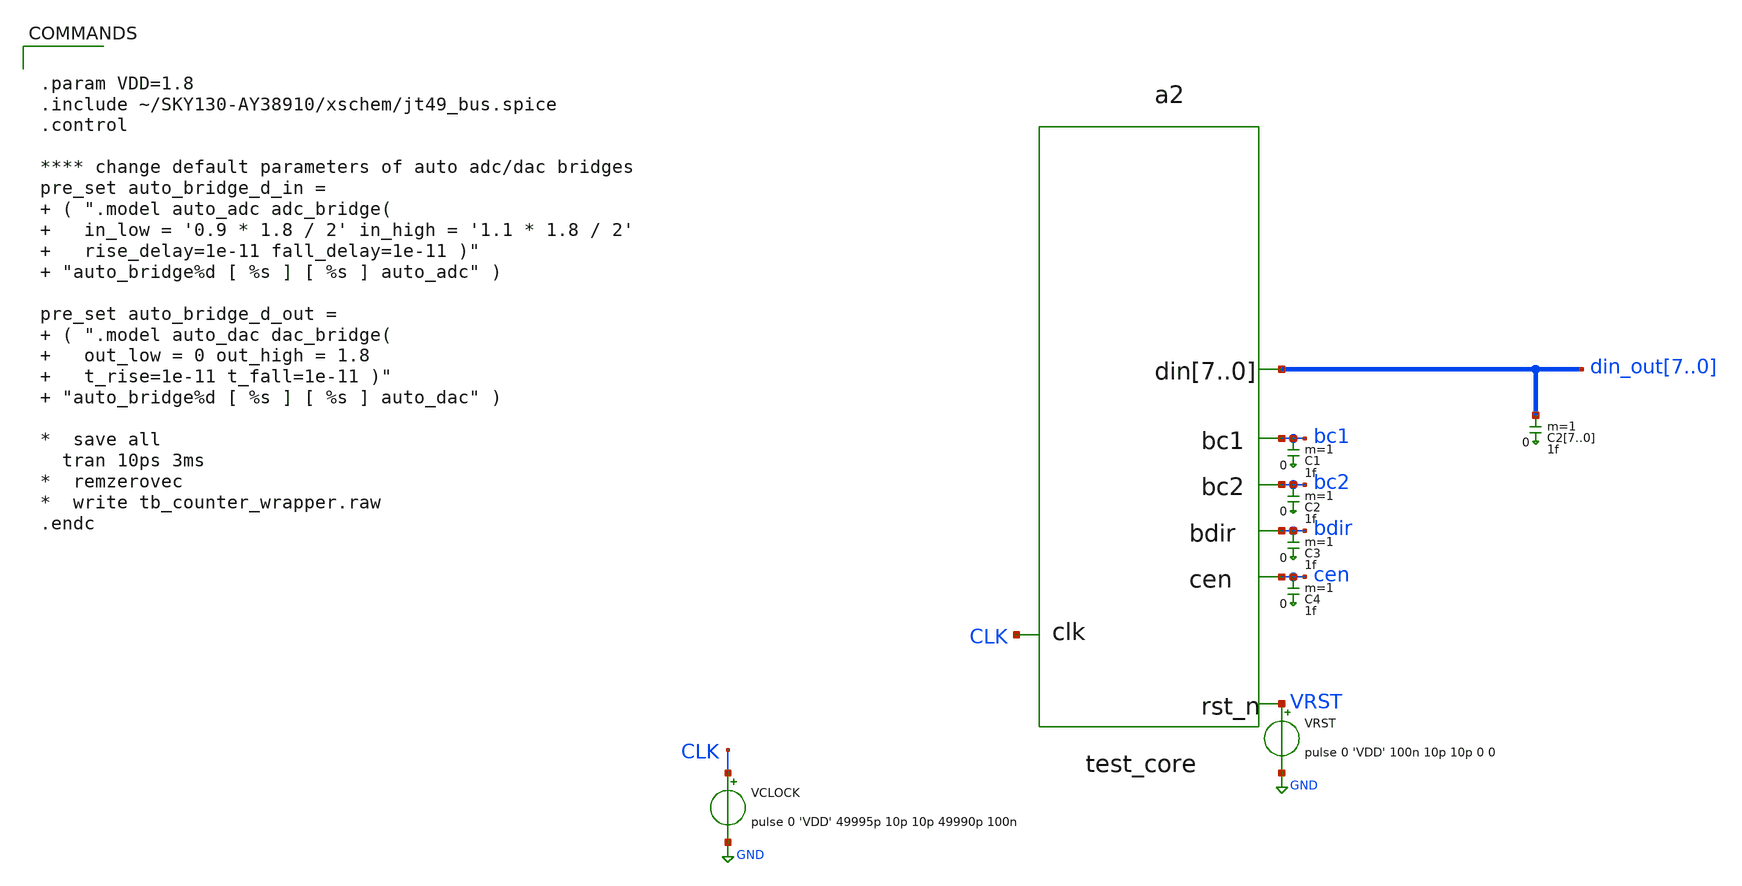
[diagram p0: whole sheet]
** sch_path: xschem/tb_test_core.sch
**.subckt tb_test_core
VRST VRST GND pulse 0 'VDD' 100n 10p 10p 0 0
a2 [ CLK VRST ] [ cen bdir bc1 bc2 din_out7 din_out6 din_out5 din_out4 din_out3 din_out2 din_out1
+ din_out0 ] test_core
VCLOCK CLK GND pulse 0 'VDD' 49995p 10p 10p 49990p 100n
C27 din_out7 0 1f m=1
C26 din_out6 0 1f m=1
C25 din_out5 0 1f m=1
C24 din_out4 0 1f m=1
C23 din_out3 0 1f m=1
C22 din_out2 0 1f m=1
C21 din_out1 0 1f m=1
C20 din_out0 0 1f m=1
C1 bc1 0 1f m=1
C2 bc2 0 1f m=1
C3 bdir 0 1f m=1
C4 cen 0 1f m=1
**** begin user architecture code


.param VDD=1.8
.include ~/SKY130-AY38910/xschem/jt49_bus.spice
.control

**** change default parameters of auto adc/dac bridges
pre_set auto_bridge_d_in =  ( ".model auto_adc adc_bridge(    in_low = '0.9 * 1.8 / 2' in_high = '1.1 * 1.8 / 2'
+    rise_delay=1e-11 fall_delay=1e-11 )"  "auto_bridge%d [ %s ] [ %s ] auto_adc" )

pre_set auto_bridge_d_out =  ( ".model auto_dac dac_bridge(    out_low = 0 out_high = 1.8
+    t_rise=1e-11 t_fall=1e-11 )"  "auto_bridge%d [ %s ] [ %s ] auto_dac" )

*  save all
  tran 10ps 3ms
*  remzerovec
*  write tb_counter_wrapper.raw
.endc


**** end user architecture code
**.ends
.GLOBAL GND
**** begin user architecture code
.model test_core d_cosim simulation="ivlng" sim_args=["test_core"] delay=0
**** end user architecture code
.end
